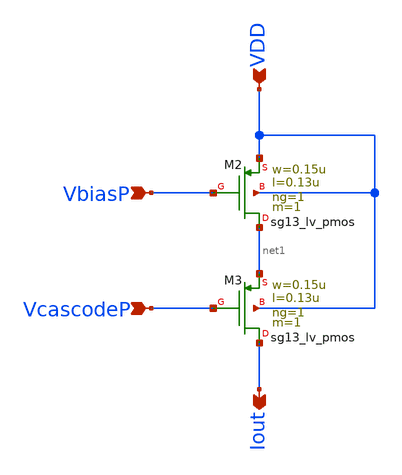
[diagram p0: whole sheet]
** sch_path: schematic/Pmirror_StdCell.sch
**.subckt Pmirror_StdCell VcascodeP VbiasP Iout VDD
*.ipin VcascodeP
*.ipin VbiasP
*.opin Iout
*.ipin VDD
XM2 net1 VbiasP VDD VDD sg13_lv_pmos w=0.15u l=0.13u ng=1 m=1 mm_ok=1
XM3 Iout VcascodeP net1 VDD sg13_lv_pmos w=0.15u l=0.13u ng=1 m=1 mm_ok=1
**.ends
.end
